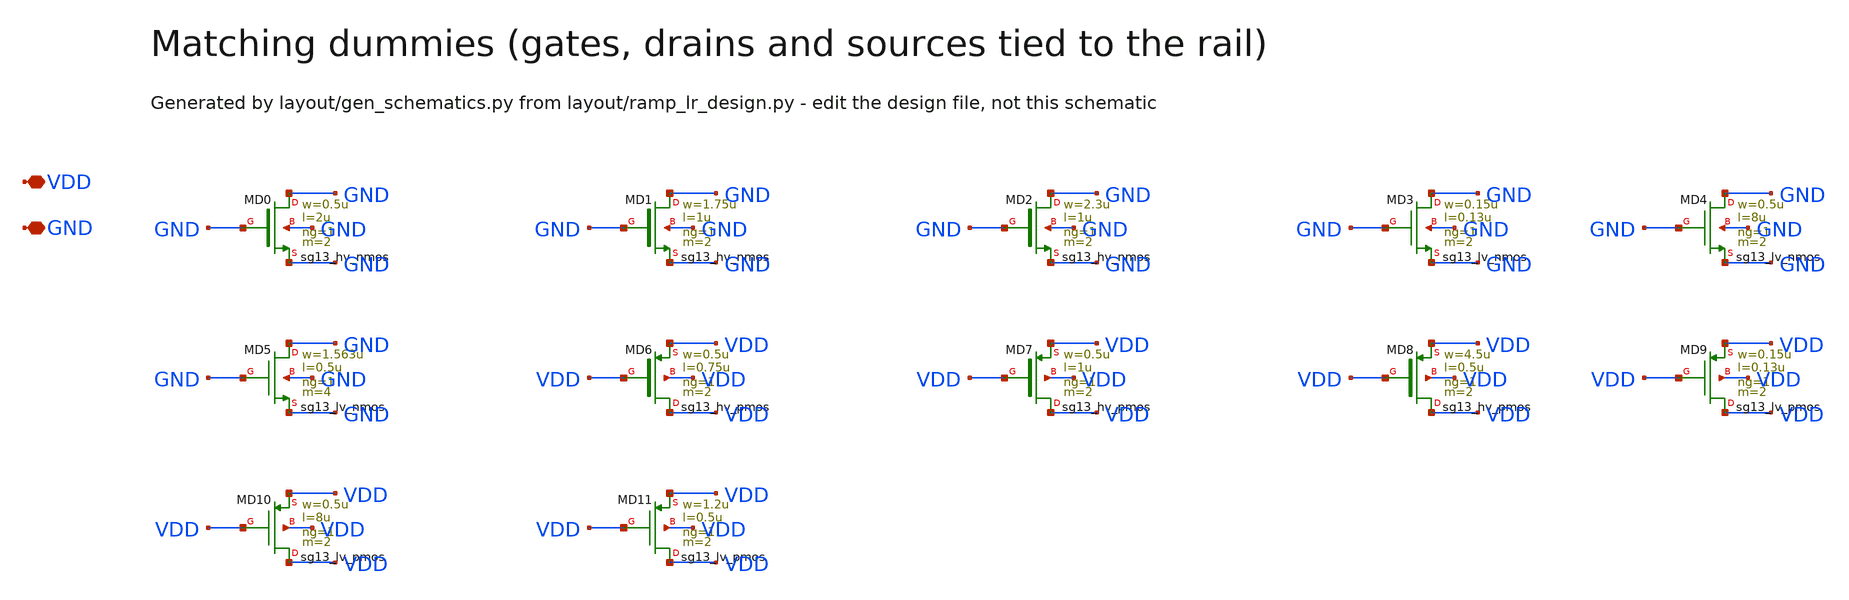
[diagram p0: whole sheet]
** sch_path: Design Files/RAMP/RAMP-LR/DUMMY_LR.sch
**.subckt DUMMY_LR VDD GND
*.iopin VDD
*.iopin GND
XMD0 GND GND GND GND sg13_hv_nmos w=0.5u l=2u ng=1 m=2 mm_ok=1
XMD1 GND GND GND GND sg13_hv_nmos w=1.75u l=1u ng=1 m=2 mm_ok=1
XMD2 GND GND GND GND sg13_hv_nmos w=2.3u l=1u ng=1 m=2 mm_ok=1
XMD3 GND GND GND GND sg13_lv_nmos w=0.15u l=0.13u ng=1 m=2 mm_ok=1
XMD4 GND GND GND GND sg13_lv_nmos w=0.5u l=8u ng=1 m=2 mm_ok=1
XMD5 GND GND GND GND sg13_lv_nmos w=1.563u l=0.5u ng=1 m=4 mm_ok=1
XMD6 VDD VDD VDD VDD sg13_hv_pmos w=0.5u l=0.75u ng=1 m=2 mm_ok=1
XMD7 VDD VDD VDD VDD sg13_hv_pmos w=0.5u l=1u ng=1 m=2 mm_ok=1
XMD8 VDD VDD VDD VDD sg13_hv_pmos w=4.5u l=0.5u ng=1 m=2 mm_ok=1
XMD9 VDD VDD VDD VDD sg13_lv_pmos w=0.15u l=0.13u ng=1 m=2 mm_ok=1
XMD10 VDD VDD VDD VDD sg13_lv_pmos w=0.5u l=8u ng=1 m=2 mm_ok=1
XMD11 VDD VDD VDD VDD sg13_lv_pmos w=1.2u l=0.5u ng=1 m=2 mm_ok=1
**.ends
.end
